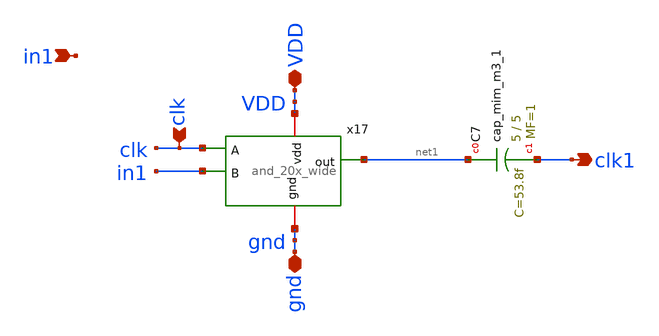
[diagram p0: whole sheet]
** sch_path: xschem/and_capacitor_5.sch
**.subckt and_capacitor_5 clk VDD gnd clk1 in1
*.ipin clk
*.iopin VDD
*.iopin gnd
*.opin clk1
*.ipin in1
x17 net1 clk in1 VDD gnd and_20x_wide
XC7 net1 clk1 sky130_fd_pr__cap_mim_m3_1 W=5 L=5 MF=1 m=1
**.ends

* expanding   symbol:  and_20x_wide.sym # of pins=5
** sym_path: xschem/and_20x_wide.sym
** sch_path: xschem/and_20x_wide.sch
.subckt and_20x_wide out A B vdd gnd
*.iopin gnd
*.iopin vdd
*.ipin A
*.ipin B
*.opin out
XM2 net1 net3 vdd vdd sky130_fd_pr__pfet_01v8 L=0.15 W=1.26 nf=1 ad='int((nf+1)/2) * W/nf * 0.29' as='int((nf+2)/2) * W/nf * 0.29'
+ pd='2*int((nf+1)/2) * (W/nf + 0.29)' ps='2*int((nf+2)/2) * (W/nf + 0.29)' nrd='0.29 / W' nrs='0.29 / W'
+ sa=0 sb=0 sd=0 mult=1 m=1
XM1 net1 B vdd vdd sky130_fd_pr__pfet_01v8 L=0.15 W=7.56 nf=1 ad='int((nf+1)/2) * W/nf * 0.29' as='int((nf+2)/2) * W/nf * 0.29'
+ pd='2*int((nf+1)/2) * (W/nf + 0.29)' ps='2*int((nf+2)/2) * (W/nf + 0.29)' nrd='0.29 / W' nrs='0.29 / W'
+ sa=0 sb=0 sd=0 mult=1 m=1
XM3 out net1 vdd vdd sky130_fd_pr__pfet_01v8 L=0.15 W=7.56 nf=1 ad='int((nf+1)/2) * W/nf * 0.29' as='int((nf+2)/2) * W/nf * 0.29'
+ pd='2*int((nf+1)/2) * (W/nf + 0.29)' ps='2*int((nf+2)/2) * (W/nf + 0.29)' nrd='0.29 / W' nrs='0.29 / W'
+ sa=0 sb=0 sd=0 mult=1 m=1
XM4 net1 net3 net2 gnd sky130_fd_pr__nfet_01v8 L=0.15 W=0.42 nf=1 ad='int((nf+1)/2) * W/nf * 0.29' as='int((nf+2)/2) * W/nf * 0.29'
+ pd='2*int((nf+1)/2) * (W/nf + 0.29)' ps='2*int((nf+2)/2) * (W/nf + 0.29)' nrd='0.29 / W' nrs='0.29 / W'
+ sa=0 sb=0 sd=0 mult=1 m=1
XM5 net2 B gnd gnd sky130_fd_pr__nfet_01v8 L=0.15 W=2.52 nf=1 ad='int((nf+1)/2) * W/nf * 0.29' as='int((nf+2)/2) * W/nf * 0.29'
+ pd='2*int((nf+1)/2) * (W/nf + 0.29)' ps='2*int((nf+2)/2) * (W/nf + 0.29)' nrd='0.29 / W' nrs='0.29 / W'
+ sa=0 sb=0 sd=0 mult=1 m=1
XM6 out net1 gnd gnd sky130_fd_pr__nfet_01v8 L=0.15 W=2.52 nf=1 ad='int((nf+1)/2) * W/nf * 0.29' as='int((nf+2)/2) * W/nf * 0.29'
+ pd='2*int((nf+1)/2) * (W/nf + 0.29)' ps='2*int((nf+2)/2) * (W/nf + 0.29)' nrd='0.29 / W' nrs='0.29 / W'
+ sa=0 sb=0 sd=0 mult=1 m=1
XM45 net3 net4 gnd gnd sky130_fd_pr__nfet_01v8 L=0.15 W=11.34 nf=1 ad='int((nf+1)/2) * W/nf * 0.29' as='int((nf+2)/2) * W/nf * 0.29'
+ pd='2*int((nf+1)/2) * (W/nf + 0.29)' ps='2*int((nf+2)/2) * (W/nf + 0.29)' nrd='0.29 / W' nrs='0.29 / W'
+ sa=0 sb=0 sd=0 mult=1 m=1
XM46 net3 net4 vdd vdd sky130_fd_pr__pfet_01v8 L=0.15 W=34.02 nf=1 ad='int((nf+1)/2) * W/nf * 0.29' as='int((nf+2)/2) * W/nf * 0.29'
+ pd='2*int((nf+1)/2) * (W/nf + 0.29)' ps='2*int((nf+2)/2) * (W/nf + 0.29)' nrd='0.29 / W' nrs='0.29 / W'
+ sa=0 sb=0 sd=0 mult=1 m=1
XM7 net4 A gnd gnd sky130_fd_pr__nfet_01v8 L=0.15 W=11.34 nf=1 ad='int((nf+1)/2) * W/nf * 0.29' as='int((nf+2)/2) * W/nf * 0.29'
+ pd='2*int((nf+1)/2) * (W/nf + 0.29)' ps='2*int((nf+2)/2) * (W/nf + 0.29)' nrd='0.29 / W' nrs='0.29 / W'
+ sa=0 sb=0 sd=0 mult=1 m=1
XM8 net4 A vdd vdd sky130_fd_pr__pfet_01v8 L=0.15 W=34.02 nf=1 ad='int((nf+1)/2) * W/nf * 0.29' as='int((nf+2)/2) * W/nf * 0.29'
+ pd='2*int((nf+1)/2) * (W/nf + 0.29)' ps='2*int((nf+2)/2) * (W/nf + 0.29)' nrd='0.29 / W' nrs='0.29 / W'
+ sa=0 sb=0 sd=0 mult=1 m=1
.ends

.end
